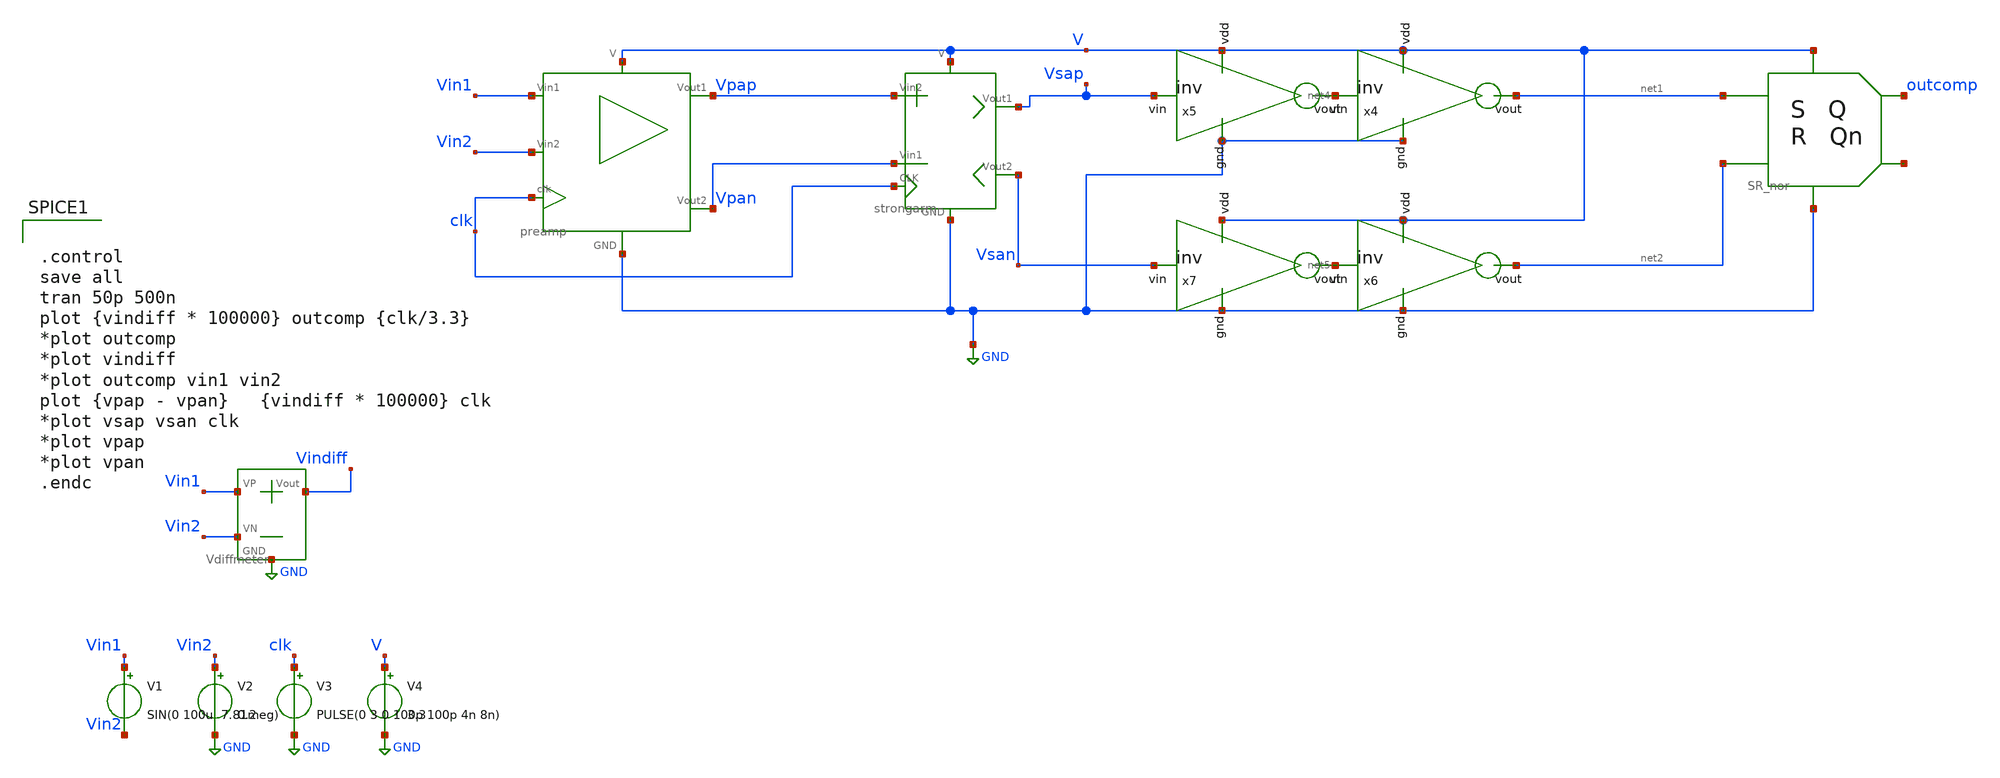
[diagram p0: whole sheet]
** sch_path: SAR_ADC/xschem/test/comp_full_tb/comp_sin_1u_10meg_tb.sch
**.subckt comp_sin_1u_10meg_tb
V1 Vin1 Vin2 SIN(0 100u 7.81meg)
V2 Vin2 GND 0.2
V3 clk GND PULSE(0 3 0 100p 100p 4n 8n)
V4 V GND 3.3
X2 Vin1 Vin2 Vindiff GND Vdiffmeter
X3 net1 V GND net2 outcomp net3 SR_nor
x4 V GND net1 net4 inv cl=0.28u wp=0.44u wn=0.22u
x5 V GND net4 Vsap inv cl=0.28u wp=0.44u wn=0.22u
x6 V GND net2 net5 inv cl=0.28u wp=0.44u wn=0.22u
x7 V GND net5 Vsan inv cl=0.28u wp=0.44u wn=0.22u
X8 V GND Vpan Vpap clk Vsap Vsan strongarm
X9 V GND Vin1 clk Vpap Vpan Vin2 preamp
**** begin user architecture code


.control
save all
tran 50p 500n
plot {vindiff * 100000} outcomp {clk/3.3}
*plot outcomp
*plot vindiff
*plot outcomp vin1 vin2
plot {vpap - vpan}   {vindiff * 100000} clk
*plot vsap vsan clk
*plot vpap
*plot vpan
.endc


.include $env(PDK_ROOT)/$env(PDK)/libs.tech/ngspice/design.ngspice
.lib $env(PDK_ROOT)/$env(PDK)/libs.tech/ngspice/sm141064.ngspice typical

**** end user architecture code
**.ends

* expanding   symbol:  Vdiffmeter.sym # of pins=4
** sym_path: SAR_ADC/xschem/designs/Vdiffmeter.sym
** sch_path: SAR_ADC/xschem/designs/Vdiffmeter.sch
.subckt Vdiffmeter VP VN Vout GND
*.iopin Vout
*.iopin GND
*.iopin VP
*.iopin VN
R4 Vout GND 1k m=1
E4 Vout GND VP VN 1
.ends


* expanding   symbol:  SR_nor.sym # of pins=6
** sym_path: SAR_ADC/xschem/designs/SR_nor.sym
** sch_path: SAR_ADC/xschem/designs/SR_nor.sch
.subckt SR_nor S V GND R Q Qn
*.iopin V
*.iopin GND
*.iopin S
*.iopin R
*.iopin Qn
*.iopin Q
X1 S Q Qn GND V norgate
X2 Qn R Q GND V norgate
.ends


* expanding   symbol:  inv.sym # of pins=4
** sym_path: SAR_ADC/xschem/spice/inv.sym
** sch_path: SAR_ADC/xschem/spice/inv.sch
.subckt inv vdd gnd vout vin  cl=0.28u wp=0.44u wn=0.22u
*.ipin gnd
*.ipin vdd
*.ipin vin
*.opin vout
XM1 gnd vin vout gnd nfet_03v3 L=0.28u W=4u nf=1 ad='int((nf+1)/2) * W/nf * 0.18u' as='int((nf+2)/2) * W/nf * 0.18u'
+ pd='2*int((nf+1)/2) * (W/nf + 0.18u)' ps='2*int((nf+2)/2) * (W/nf + 0.18u)' nrd='0.18u / W' nrs='0.18u / W'
+ sa=0 sb=0 sd=0 m=1
XM2 vdd vin vout vdd pfet_03v3 L=0.28u W=4u nf=1 ad='int((nf+1)/2) * W/nf * 0.18u' as='int((nf+2)/2) * W/nf * 0.18u'
+ pd='2*int((nf+1)/2) * (W/nf + 0.18u)' ps='2*int((nf+2)/2) * (W/nf + 0.18u)' nrd='0.18u / W' nrs='0.18u / W'
+ sa=0 sb=0 sd=0 m=1
.ends


* expanding   symbol:  strongarm.sym # of pins=7
** sym_path: SAR_ADC/xschem/designs/strongarm.sym
** sch_path: SAR_ADC/xschem/designs/strongarm.sch
.subckt strongarm V GND Vin1 Vin2 CLK Vout1 Vout2
*.iopin V
*.iopin Vout1
*.iopin Vin1
*.iopin Vin2
*.iopin Vout2
*.iopin CLK
*.iopin GND
XM1 net3 Vout2 V V pfet_03v3 L=0.28u W=2u nf=1 ad='int((nf+1)/2) * W/nf * 0.18u' as='int((nf+2)/2) * W/nf * 0.18u'
+ pd='2*int((nf+1)/2) * (W/nf + 0.18u)' ps='2*int((nf+2)/2) * (W/nf + 0.18u)' nrd='0.18u / W' nrs='0.18u / W'
+ sa=0 sb=0 sd=0 m=1
XM2 Vout1 net1 GND GND nfet_03v3 L=0.28u W=2u nf=1 ad='int((nf+1)/2) * W/nf * 0.18u' as='int((nf+2)/2) * W/nf * 0.18u'
+ pd='2*int((nf+1)/2) * (W/nf + 0.18u)' ps='2*int((nf+2)/2) * (W/nf + 0.18u)' nrd='0.18u / W' nrs='0.18u / W'
+ sa=0 sb=0 sd=0 m=1
XM3 Vout2 Vout1 GND GND nfet_03v3 L=0.28u W=2u nf=1 ad='int((nf+1)/2) * W/nf * 0.18u' as='int((nf+2)/2) * W/nf * 0.18u'
+ pd='2*int((nf+1)/2) * (W/nf + 0.18u)' ps='2*int((nf+2)/2) * (W/nf + 0.18u)' nrd='0.18u / W' nrs='0.18u / W'
+ sa=0 sb=0 sd=0 m=1
XM4 Vout2 net1 GND GND nfet_03v3 L=0.28u W=2u nf=1 ad='int((nf+1)/2) * W/nf * 0.18u' as='int((nf+2)/2) * W/nf * 0.18u'
+ pd='2*int((nf+1)/2) * (W/nf + 0.18u)' ps='2*int((nf+2)/2) * (W/nf + 0.18u)' nrd='0.18u / W' nrs='0.18u / W'
+ sa=0 sb=0 sd=0 m=1
XM5 Vout1 Vout2 GND GND nfet_03v3 L=0.28u W=2u nf=1 ad='int((nf+1)/2) * W/nf * 0.18u' as='int((nf+2)/2) * W/nf * 0.18u'
+ pd='2*int((nf+1)/2) * (W/nf + 0.18u)' ps='2*int((nf+2)/2) * (W/nf + 0.18u)' nrd='0.18u / W' nrs='0.18u / W'
+ sa=0 sb=0 sd=0 m=1
XM6 net2 Vout1 V V pfet_03v3 L=0.28u W=2u nf=1 ad='int((nf+1)/2) * W/nf * 0.18u' as='int((nf+2)/2) * W/nf * 0.18u'
+ pd='2*int((nf+1)/2) * (W/nf + 0.18u)' ps='2*int((nf+2)/2) * (W/nf + 0.18u)' nrd='0.18u / W' nrs='0.18u / W'
+ sa=0 sb=0 sd=0 m=1
XM7 Vout1 Vin1 net3 V pfet_03v3 L=0.28u W=10u nf=1 ad='int((nf+1)/2) * W/nf * 0.18u' as='int((nf+2)/2) * W/nf * 0.18u'
+ pd='2*int((nf+1)/2) * (W/nf + 0.18u)' ps='2*int((nf+2)/2) * (W/nf + 0.18u)' nrd='0.18u / W' nrs='0.18u / W'
+ sa=0 sb=0 sd=0 m=1
XM8 Vout2 Vin2 net2 V pfet_03v3 L=0.28u W=10u nf=1 ad='int((nf+1)/2) * W/nf * 0.18u' as='int((nf+2)/2) * W/nf * 0.18u'
+ pd='2*int((nf+1)/2) * (W/nf + 0.18u)' ps='2*int((nf+2)/2) * (W/nf + 0.18u)' nrd='0.18u / W' nrs='0.18u / W'
+ sa=0 sb=0 sd=0 m=1
x1 V GND net4 CLK inv cl=0.28u wp=0.44u wn=0.22u wx=4u
x2 V GND net1 net4 inv cl=0.28u wp=0.44u wn=0.22u wx=4u
.ends


* expanding   symbol:  preamp.sym # of pins=7
** sym_path: SAR_ADC/xschem/designs/preamp.sym
** sch_path: SAR_ADC/xschem/designs/preamp.sch
.subckt preamp V GND Vin1 clk Vout1 Vout2 Vin2
*.iopin V
*.iopin GND
*.iopin Vout2
*.iopin Vout1
*.iopin clk
*.iopin Vin2
*.iopin Vin1
XM26 Vout2 clk GND GND nfet_03v3 L=.5u W=.22u nf=1 ad='int((nf+1)/2) * W/nf * 0.18u' as='int((nf+2)/2) * W/nf * 0.18u'
+ pd='2*int((nf+1)/2) * (W/nf + 0.18u)' ps='2*int((nf+2)/2) * (W/nf + 0.18u)' nrd='0.18u / W' nrs='0.18u / W'
+ sa=0 sb=0 sd=0 m=1
XM27 Vout1 clk GND GND nfet_03v3 L=.5u W=.22u nf=1 ad='int((nf+1)/2) * W/nf * 0.18u' as='int((nf+2)/2) * W/nf * 0.18u'
+ pd='2*int((nf+1)/2) * (W/nf + 0.18u)' ps='2*int((nf+2)/2) * (W/nf + 0.18u)' nrd='0.18u / W' nrs='0.18u / W'
+ sa=0 sb=0 sd=0 m=1
XM24 Vout1 Vin2 net1 V pfet_03v3 L=.28u W=8u nf=1 ad='int((nf+1)/2) * W/nf * 0.18u' as='int((nf+2)/2) * W/nf * 0.18u'
+ pd='2*int((nf+1)/2) * (W/nf + 0.18u)' ps='2*int((nf+2)/2) * (W/nf + 0.18u)' nrd='0.18u / W' nrs='0.18u / W'
+ sa=0 sb=0 sd=0 m=1
XM25 Vout2 Vin1 net1 V pfet_03v3 L=.28u W=8u nf=1 ad='int((nf+1)/2) * W/nf * 0.18u' as='int((nf+2)/2) * W/nf * 0.18u'
+ pd='2*int((nf+1)/2) * (W/nf + 0.18u)' ps='2*int((nf+2)/2) * (W/nf + 0.18u)' nrd='0.18u / W' nrs='0.18u / W'
+ sa=0 sb=0 sd=0 m=1
XM1 V clk net1 V pfet_03v3 L=2u W=1u nf=1 ad='int((nf+1)/2) * W/nf * 0.18u' as='int((nf+2)/2) * W/nf * 0.18u'
+ pd='2*int((nf+1)/2) * (W/nf + 0.18u)' ps='2*int((nf+2)/2) * (W/nf + 0.18u)' nrd='0.18u / W' nrs='0.18u / W'
+ sa=0 sb=0 sd=0 m=1
.ends


* expanding   symbol:  norgate.sym # of pins=5
** sym_path: SAR_ADC/xschem/designs/norgate.sym
** sch_path: SAR_ADC/xschem/designs/norgate.sch
.subckt norgate A B Z GND V
*.iopin GND
*.iopin A
*.iopin B
*.iopin V
*.iopin Z
XM3 V A net2 V pfet_03v3 L=0.28u W=0.22u nf=1 ad='int((nf+1)/2) * W/nf * 0.18u' as='int((nf+2)/2) * W/nf * 0.18u'
+ pd='2*int((nf+1)/2) * (W/nf + 0.18u)' ps='2*int((nf+2)/2) * (W/nf + 0.18u)' nrd='0.18u / W' nrs='0.18u / W'
+ sa=0 sb=0 sd=0 m=1
XM6 net2 B Z V pfet_03v3 L=0.28u W=0.22u nf=1 ad='int((nf+1)/2) * W/nf * 0.18u' as='int((nf+2)/2) * W/nf * 0.18u'
+ pd='2*int((nf+1)/2) * (W/nf + 0.18u)' ps='2*int((nf+2)/2) * (W/nf + 0.18u)' nrd='0.18u / W' nrs='0.18u / W'
+ sa=0 sb=0 sd=0 m=1
XM9 V B net1 V pfet_03v3 L=0.28u W=0.22u nf=1 ad='int((nf+1)/2) * W/nf * 0.18u' as='int((nf+2)/2) * W/nf * 0.18u'
+ pd='2*int((nf+1)/2) * (W/nf + 0.18u)' ps='2*int((nf+2)/2) * (W/nf + 0.18u)' nrd='0.18u / W' nrs='0.18u / W'
+ sa=0 sb=0 sd=0 m=1
XM12 net1 A Z V pfet_03v3 L=0.28u W=0.22u nf=1 ad='int((nf+1)/2) * W/nf * 0.18u' as='int((nf+2)/2) * W/nf * 0.18u'
+ pd='2*int((nf+1)/2) * (W/nf + 0.18u)' ps='2*int((nf+2)/2) * (W/nf + 0.18u)' nrd='0.18u / W' nrs='0.18u / W'
+ sa=0 sb=0 sd=0 m=1
XM2 Z B GND GND nfet_03v3 L=0.28u W=0.22u nf=1 ad='int((nf+1)/2) * W/nf * 0.18u' as='int((nf+2)/2) * W/nf * 0.18u'
+ pd='2*int((nf+1)/2) * (W/nf + 0.18u)' ps='2*int((nf+2)/2) * (W/nf + 0.18u)' nrd='0.18u / W' nrs='0.18u / W'
+ sa=0 sb=0 sd=0 m=1
XM4 Z A GND GND nfet_03v3 L=0.28u W=0.22u nf=1 ad='int((nf+1)/2) * W/nf * 0.18u' as='int((nf+2)/2) * W/nf * 0.18u'
+ pd='2*int((nf+1)/2) * (W/nf + 0.18u)' ps='2*int((nf+2)/2) * (W/nf + 0.18u)' nrd='0.18u / W' nrs='0.18u / W'
+ sa=0 sb=0 sd=0 m=1
.ends

.GLOBAL GND
.end
